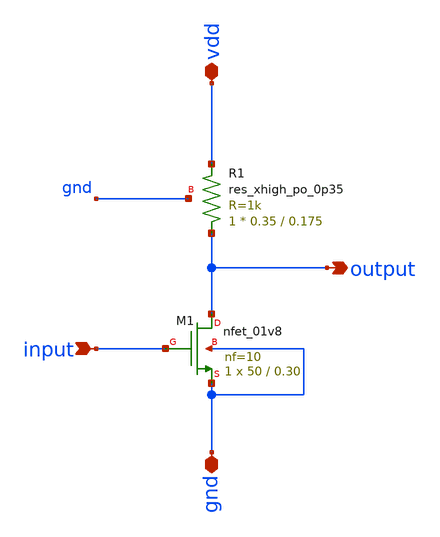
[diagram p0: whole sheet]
** sch_path: xschem/cs_amplifier.sch
**.subckt cs_amplifier input vdd gnd output
*.ipin input
*.iopin vdd
*.iopin gnd
*.opin output
XM1 output input gnd gnd sky130_fd_pr__nfet_01v8 L=0.30 W=50 nf=10 ad='int((nf+1)/2) * W/nf * 0.29' as='int((nf+2)/2) * W/nf * 0.29'
+ pd='2*int((nf+1)/2) * (W/nf + 0.29)' ps='2*int((nf+2)/2) * (W/nf + 0.29)' nrd='0.29 / W' nrs='0.29 / W'
+ sa=0 sb=0 sd=0 mult=1 m=1
XR1 output vdd gnd sky130_fd_pr__res_xhigh_po_0p35 L=0.175 mult=1 m=1
**.ends
.end
